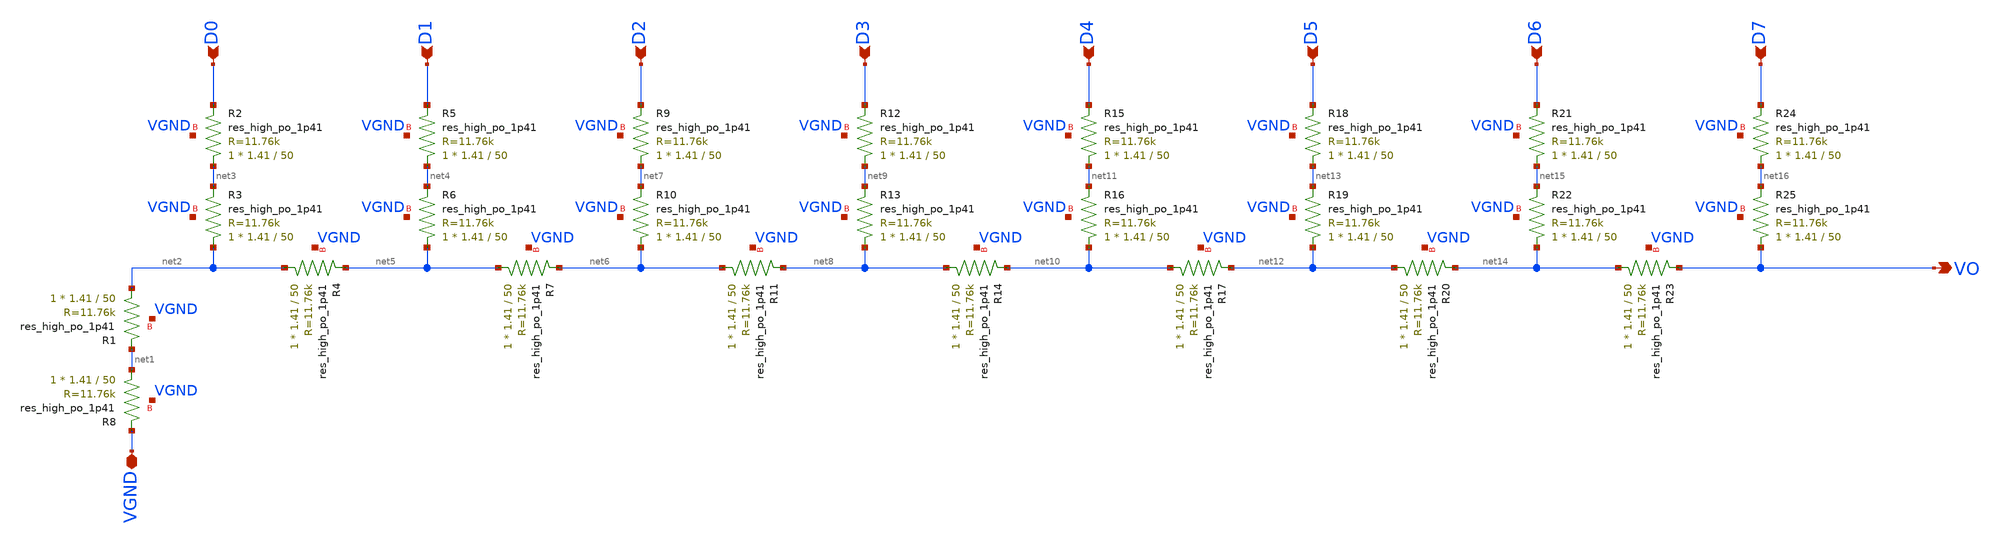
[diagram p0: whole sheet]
** sch_path: xschem/r2r.sch
**.subckt r2r D0 D1 D2 D3 D4 D5 D6 D7 VO VGND
*.ipin D0
*.ipin D1
*.ipin D2
*.ipin D3
*.ipin D4
*.ipin D5
*.ipin D6
*.ipin D7
*.opin VO
*.iopin VGND
XR8 net1 VGND VGND sky130_fd_pr__res_high_po_1p41 L=50 mult=1 m=1
XR1 net2 net1 VGND sky130_fd_pr__res_high_po_1p41 L=50 mult=1 m=1
XR2 net3 D0 VGND sky130_fd_pr__res_high_po_1p41 L=50 mult=1 m=1
XR3 net2 net3 VGND sky130_fd_pr__res_high_po_1p41 L=50 mult=1 m=1
XR4 net2 net5 VGND sky130_fd_pr__res_high_po_1p41 L=50 mult=1 m=1
XR5 net4 D1 VGND sky130_fd_pr__res_high_po_1p41 L=50 mult=1 m=1
XR6 net5 net4 VGND sky130_fd_pr__res_high_po_1p41 L=50 mult=1 m=1
XR7 net5 net6 VGND sky130_fd_pr__res_high_po_1p41 L=50 mult=1 m=1
XR9 net7 D2 VGND sky130_fd_pr__res_high_po_1p41 L=50 mult=1 m=1
XR10 net6 net7 VGND sky130_fd_pr__res_high_po_1p41 L=50 mult=1 m=1
XR11 net6 net8 VGND sky130_fd_pr__res_high_po_1p41 L=50 mult=1 m=1
XR12 net9 D3 VGND sky130_fd_pr__res_high_po_1p41 L=50 mult=1 m=1
XR13 net8 net9 VGND sky130_fd_pr__res_high_po_1p41 L=50 mult=1 m=1
XR14 net8 net10 VGND sky130_fd_pr__res_high_po_1p41 L=50 mult=1 m=1
XR15 net11 D4 VGND sky130_fd_pr__res_high_po_1p41 L=50 mult=1 m=1
XR16 net10 net11 VGND sky130_fd_pr__res_high_po_1p41 L=50 mult=1 m=1
XR17 net10 net12 VGND sky130_fd_pr__res_high_po_1p41 L=50 mult=1 m=1
XR18 net13 D5 VGND sky130_fd_pr__res_high_po_1p41 L=50 mult=1 m=1
XR19 net12 net13 VGND sky130_fd_pr__res_high_po_1p41 L=50 mult=1 m=1
XR20 net12 net14 VGND sky130_fd_pr__res_high_po_1p41 L=50 mult=1 m=1
XR21 net15 D6 VGND sky130_fd_pr__res_high_po_1p41 L=50 mult=1 m=1
XR22 net14 net15 VGND sky130_fd_pr__res_high_po_1p41 L=50 mult=1 m=1
XR23 net14 VO VGND sky130_fd_pr__res_high_po_1p41 L=50 mult=1 m=1
XR24 net16 D7 VGND sky130_fd_pr__res_high_po_1p41 L=50 mult=1 m=1
XR25 VO net16 VGND sky130_fd_pr__res_high_po_1p41 L=50 mult=1 m=1
**.ends
.end
